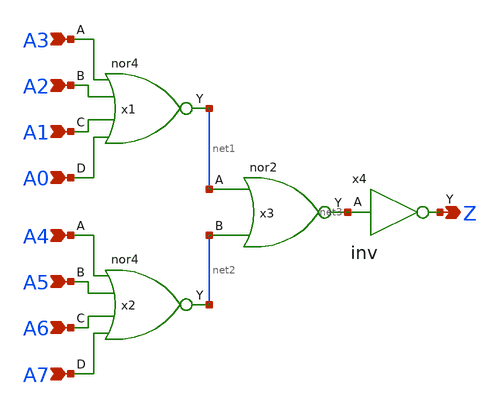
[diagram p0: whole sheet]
** sch_path: design/xschem/ZV_FLAG/Z_FLAG.sch
**.subckt Z_FLAG Z A4 A5 A6 A7 A0 A3 A2 A1
*.opin Z
*.ipin A4
*.ipin A5
*.ipin A6
*.ipin A7
*.ipin A0
*.ipin A3
*.ipin A2
*.ipin A1
x1 A3 A2 A1 A0 VSS VDD net1 nor4
x2 A4 A5 A6 A7 VSS VDD net2 nor4
x3 net1 net2 VSS VDD net3 nor2
x4 net3 VSS VDD Z inv
**.ends
.end
